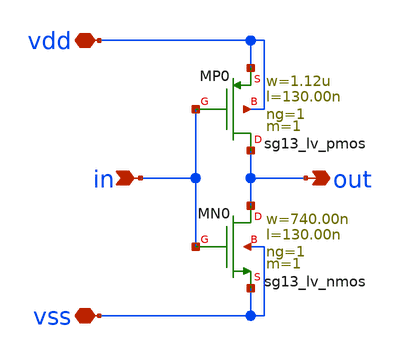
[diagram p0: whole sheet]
** sch_path: challenges/demo-cmos-inverter-layout/inverter.sch
**.subckt inverter out in vdd vss
*.opin out
*.ipin in
*.iopin vdd
*.iopin vss
XMN0 out in vss vss sg13_lv_nmos w=740.00n l=130.00n ng=1 m=1 mm_ok=1
XMP0 out in vdd vdd sg13_lv_pmos w=1.12u l=130.00n ng=1 m=1 mm_ok=1
**.ends
.end
